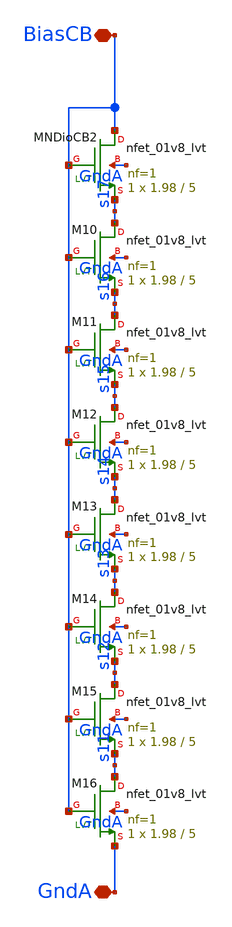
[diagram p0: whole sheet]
** sch_path: analog/klayout/production/final_merge_20260923/testbenches/cace/analog/xschem/BiasCoarseMB_DIV_W019_L050_8.sch
**.subckt BiasCoarseMB_DIV_W019_L050_8 GndA BiasCB
*.iopin GndA
*.iopin BiasCB
XMNDioCB2 BiasCB BiasCB s17 GndA sky130_fd_pr__nfet_01v8_lvt L=5 W=1.98 nf=1 ad='int((1 + 1)/2) * 1.98 / 1 * 0.29'
+ as='int((1 + 2)/2) * 1.98 / 1 * 0.29' pd='2*int((1 + 1)/2) * (1.98 / 1 + 0.29)' ps='2*int((1 + 2)/2) * (1.98 / 1 + 0.29)'
+ nrd='0.29 / 1.98 ' nrs='0.29 / 1.98 ' sa=0 sb=0 sd=0 mult=1 m=1
XM10 s17 BiasCB s16 GndA sky130_fd_pr__nfet_01v8_lvt L=5 W=1.98 nf=1 ad='int((1 + 1)/2) * 1.98 / 1 * 0.29'
+ as='int((1 + 2)/2) * 1.98 / 1 * 0.29' pd='2*int((1 + 1)/2) * (1.98 / 1 + 0.29)' ps='2*int((1 + 2)/2) * (1.98 / 1 + 0.29)'
+ nrd='0.29 / 1.98 ' nrs='0.29 / 1.98 ' sa=0 sb=0 sd=0 mult=1 m=1
XM11 s16 BiasCB s15 GndA sky130_fd_pr__nfet_01v8_lvt L=5 W=1.98 nf=1 ad='int((1 + 1)/2) * 1.98 / 1 * 0.29'
+ as='int((1 + 2)/2) * 1.98 / 1 * 0.29' pd='2*int((1 + 1)/2) * (1.98 / 1 + 0.29)' ps='2*int((1 + 2)/2) * (1.98 / 1 + 0.29)'
+ nrd='0.29 / 1.98 ' nrs='0.29 / 1.98 ' sa=0 sb=0 sd=0 mult=1 m=1
XM12 s15 BiasCB s14 GndA sky130_fd_pr__nfet_01v8_lvt L=5 W=1.98 nf=1 ad='int((1 + 1)/2) * 1.98 / 1 * 0.29'
+ as='int((1 + 2)/2) * 1.98 / 1 * 0.29' pd='2*int((1 + 1)/2) * (1.98 / 1 + 0.29)' ps='2*int((1 + 2)/2) * (1.98 / 1 + 0.29)'
+ nrd='0.29 / 1.98 ' nrs='0.29 / 1.98 ' sa=0 sb=0 sd=0 mult=1 m=1
XM13 s14 BiasCB s13 GndA sky130_fd_pr__nfet_01v8_lvt L=5 W=1.98 nf=1 ad='int((1 + 1)/2) * 1.98 / 1 * 0.29'
+ as='int((1 + 2)/2) * 1.98 / 1 * 0.29' pd='2*int((1 + 1)/2) * (1.98 / 1 + 0.29)' ps='2*int((1 + 2)/2) * (1.98 / 1 + 0.29)'
+ nrd='0.29 / 1.98 ' nrs='0.29 / 1.98 ' sa=0 sb=0 sd=0 mult=1 m=1
XM14 s13 BiasCB s12 GndA sky130_fd_pr__nfet_01v8_lvt L=5 W=1.98 nf=1 ad='int((1 + 1)/2) * 1.98 / 1 * 0.29'
+ as='int((1 + 2)/2) * 1.98 / 1 * 0.29' pd='2*int((1 + 1)/2) * (1.98 / 1 + 0.29)' ps='2*int((1 + 2)/2) * (1.98 / 1 + 0.29)'
+ nrd='0.29 / 1.98 ' nrs='0.29 / 1.98 ' sa=0 sb=0 sd=0 mult=1 m=1
XM15 s12 BiasCB s11 GndA sky130_fd_pr__nfet_01v8_lvt L=5 W=1.98 nf=1 ad='int((1 + 1)/2) * 1.98 / 1 * 0.29'
+ as='int((1 + 2)/2) * 1.98 / 1 * 0.29' pd='2*int((1 + 1)/2) * (1.98 / 1 + 0.29)' ps='2*int((1 + 2)/2) * (1.98 / 1 + 0.29)'
+ nrd='0.29 / 1.98 ' nrs='0.29 / 1.98 ' sa=0 sb=0 sd=0 mult=1 m=1
XM16 s11 BiasCB GndA GndA sky130_fd_pr__nfet_01v8_lvt L=5 W=1.98 nf=1 ad='int((1 + 1)/2) * 1.98 / 1 * 0.29'
+ as='int((1 + 2)/2) * 1.98 / 1 * 0.29' pd='2*int((1 + 1)/2) * (1.98 / 1 + 0.29)' ps='2*int((1 + 2)/2) * (1.98 / 1 + 0.29)'
+ nrd='0.29 / 1.98 ' nrs='0.29 / 1.98 ' sa=0 sb=0 sd=0 mult=1 m=1
**.ends
.end
